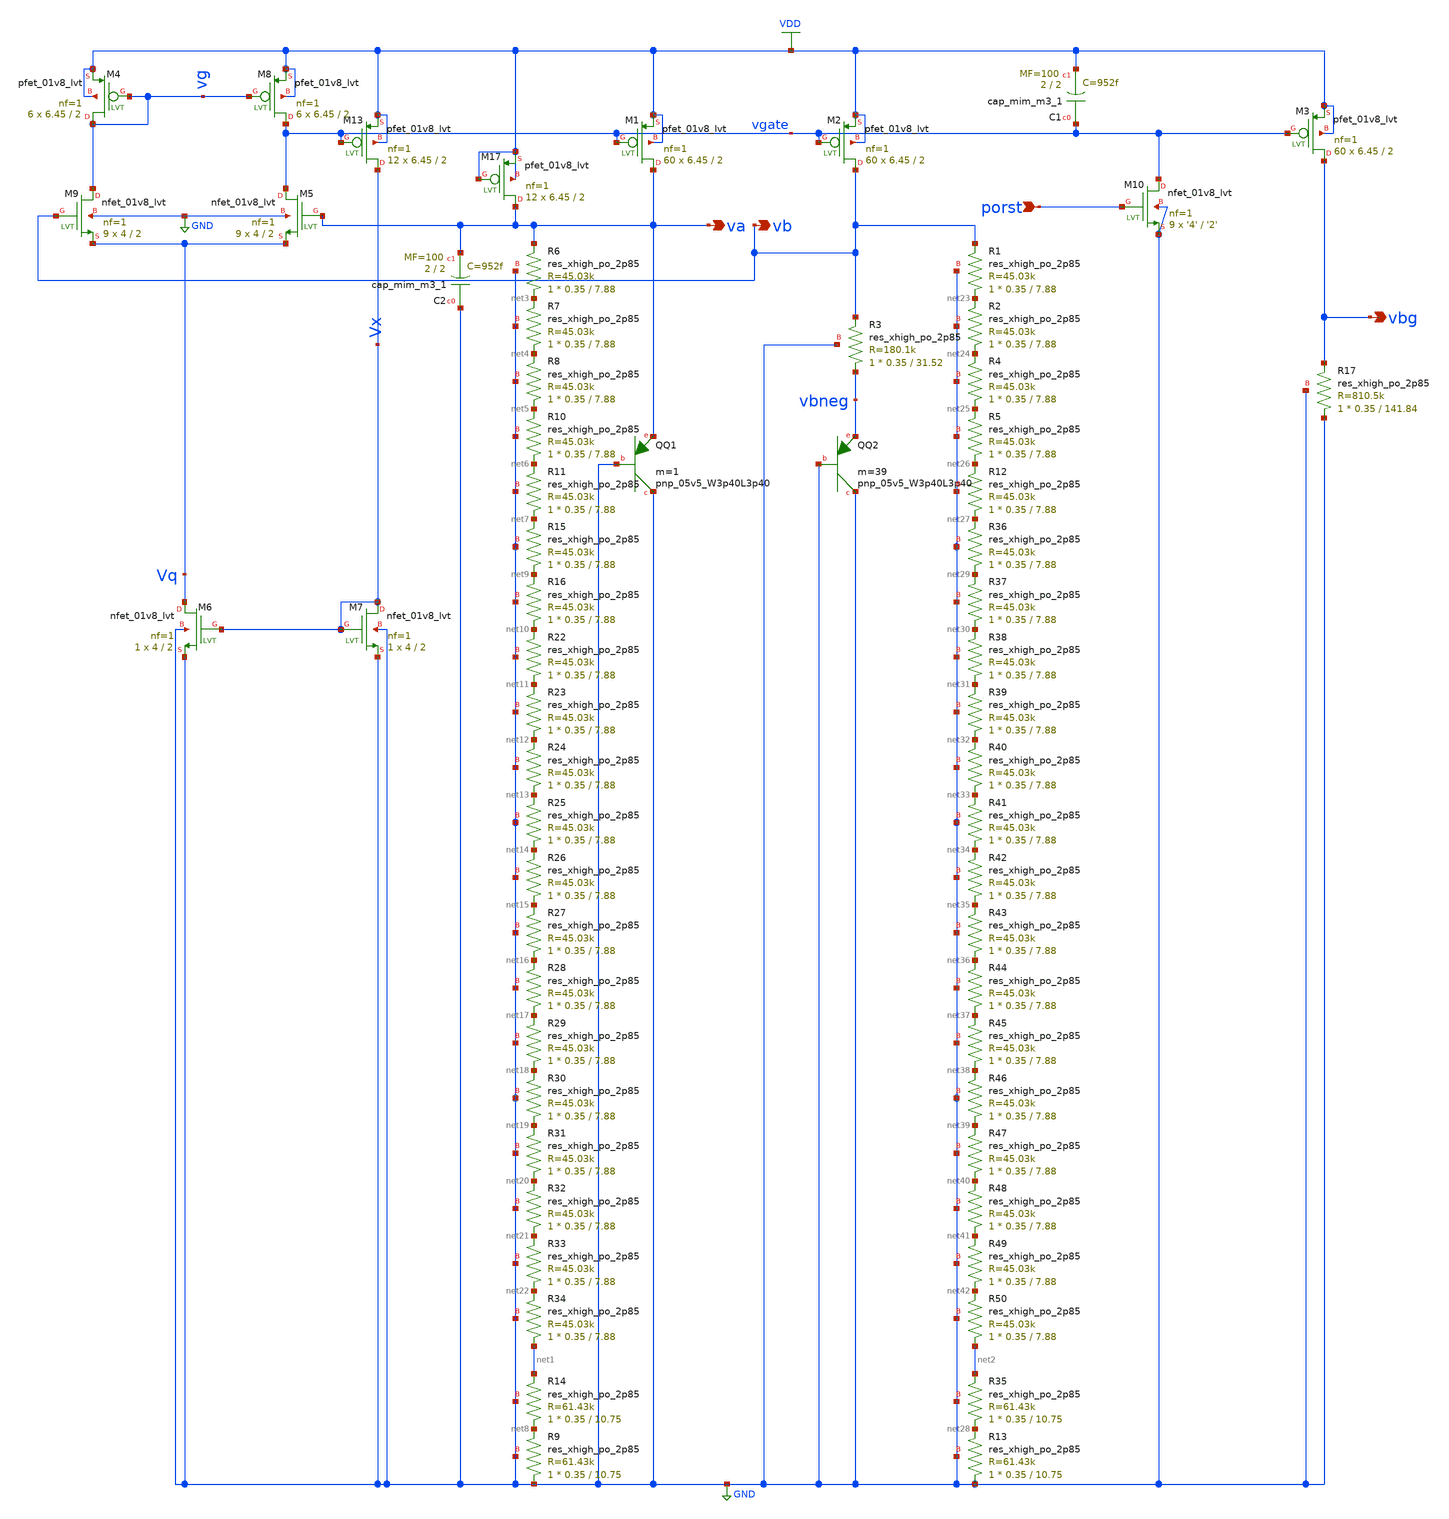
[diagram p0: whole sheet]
** sch_path: schematic/tsmc_bandgap_real_lvs.sch
**.subckt tsmc_bandgap_real_lvs porst vbg va vb
*.ipin porst
*.opin vbg
*.opin va
*.opin vb
XM5 vgate va Vq GND sky130_fd_pr__nfet_01v8_lvt L=2 W=4 nf=1 ad='int((nf+1)/2) * W/nf * 0.29' as='int((nf+2)/2) * W/nf * 0.29'
+ pd='2*int((nf+1)/2) * (W/nf + 0.29)' ps='2*int((nf+2)/2) * (W/nf + 0.29)' nrd='0.29 / W' nrs='0.29 / W'
+ sa=0 sb=0 sd=0 mult=9 m=9
XM6 Vq Vx GND GND sky130_fd_pr__nfet_01v8_lvt L=2 W=4 nf=1 ad='int((nf+1)/2) * W/nf * 0.29' as='int((nf+2)/2) * W/nf * 0.29'
+ pd='2*int((nf+1)/2) * (W/nf + 0.29)' ps='2*int((nf+2)/2) * (W/nf + 0.29)' nrd='0.29 / W' nrs='0.29 / W'
+ sa=0 sb=0 sd=0 mult=1 m=1
XM9 vg vb Vq GND sky130_fd_pr__nfet_01v8_lvt L=2 W=4 nf=1 ad='int((nf+1)/2) * W/nf * 0.29' as='int((nf+2)/2) * W/nf * 0.29'
+ pd='2*int((nf+1)/2) * (W/nf + 0.29)' ps='2*int((nf+2)/2) * (W/nf + 0.29)' nrd='0.29 / W' nrs='0.29 / W'
+ sa=0 sb=0 sd=0 mult=9 m=9
XM7 Vx Vx GND GND sky130_fd_pr__nfet_01v8_lvt L=2 W=4 nf=1 ad='int((nf+1)/2) * W/nf * 0.29' as='int((nf+2)/2) * W/nf * 0.29'
+ pd='2*int((nf+1)/2) * (W/nf + 0.29)' ps='2*int((nf+2)/2) * (W/nf + 0.29)' nrd='0.29 / W' nrs='0.29 / W'
+ sa=0 sb=0 sd=0 mult=1 m=1
XM13 Vx vgate VDD VDD sky130_fd_pr__pfet_01v8_lvt L=2 W=6.45 nf=1 ad='int((nf+1)/2) * W/nf * 0.29' as='int((nf+2)/2) * W/nf * 0.29'
+ pd='2*int((nf+1)/2) * (W/nf + 0.29)' ps='2*int((nf+2)/2) * (W/nf + 0.29)' nrd='0.29 / W' nrs='0.29 / W'
+ sa=0 sb=0 sd=0 mult=12 m=12
XM1 va vgate VDD VDD sky130_fd_pr__pfet_01v8_lvt L=2 W=6.45 nf=1 ad='int((nf+1)/2) * W/nf * 0.29' as='int((nf+2)/2) * W/nf * 0.29'
+ pd='2*int((nf+1)/2) * (W/nf + 0.29)' ps='2*int((nf+2)/2) * (W/nf + 0.29)' nrd='0.29 / W' nrs='0.29 / W'
+ sa=0 sb=0 sd=0 mult=60 m=60
XM2 vb vgate VDD VDD sky130_fd_pr__pfet_01v8_lvt L=2 W=6.45 nf=1 ad='int((nf+1)/2) * W/nf * 0.29' as='int((nf+2)/2) * W/nf * 0.29'
+ pd='2*int((nf+1)/2) * (W/nf + 0.29)' ps='2*int((nf+2)/2) * (W/nf + 0.29)' nrd='0.29 / W' nrs='0.29 / W'
+ sa=0 sb=0 sd=0 mult=60 m=60
XM3 vbg vgate VDD VDD sky130_fd_pr__pfet_01v8_lvt L=2 W=6.45 nf=1 ad='int((nf+1)/2) * W/nf * 0.29' as='int((nf+2)/2) * W/nf * 0.29'
+ pd='2*int((nf+1)/2) * (W/nf + 0.29)' ps='2*int((nf+2)/2) * (W/nf + 0.29)' nrd='0.29 / W' nrs='0.29 / W'
+ sa=0 sb=0 sd=0 mult=60 m=60
XM4 vg vg VDD VDD sky130_fd_pr__pfet_01v8_lvt L=2 W=6.45 nf=1 ad='int((nf+1)/2) * W/nf * 0.29' as='int((nf+2)/2) * W/nf * 0.29'
+ pd='2*int((nf+1)/2) * (W/nf + 0.29)' ps='2*int((nf+2)/2) * (W/nf + 0.29)' nrd='0.29 / W' nrs='0.29 / W'
+ sa=0 sb=0 sd=0 mult=6 m=6
XM8 vgate vg VDD VDD sky130_fd_pr__pfet_01v8_lvt L=2 W=6.45 nf=1 ad='int((nf+1)/2) * W/nf * 0.29' as='int((nf+2)/2) * W/nf * 0.29'
+ pd='2*int((nf+1)/2) * (W/nf + 0.29)' ps='2*int((nf+2)/2) * (W/nf + 0.29)' nrd='0.29 / W' nrs='0.29 / W'
+ sa=0 sb=0 sd=0 mult=6 m=6
XM10 vgate porst GND GND sky130_fd_pr__nfet_01v8_lvt L='2' W='4' nf=1 ad='int((nf+1)/2) * W/nf * 0.29'
+ as='int((nf+2)/2) * W/nf * 0.29' pd='2*int((nf+1)/2) * (W/nf + 0.29)' ps='2*int((nf+2)/2) * (W/nf + 0.29)'
+ nrd='0.29 / W' nrs='0.29 / W' sa=0 sb=0 sd=0 mult=9 m=9
XR6 net3 va GND sky130_fd_pr__res_xhigh_po_2p85 L=7.88 mult=1 m=1
XR7 net4 net3 GND sky130_fd_pr__res_xhigh_po_2p85 L=7.88 mult=1 m=1
XR8 net5 net4 GND sky130_fd_pr__res_xhigh_po_2p85 L=7.88 mult=1 m=1
XR10 net6 net5 GND sky130_fd_pr__res_xhigh_po_2p85 L=7.88 mult=1 m=1
XR11 net7 net6 GND sky130_fd_pr__res_xhigh_po_2p85 L=7.88 mult=1 m=1
XR9 GND net8 GND sky130_fd_pr__res_xhigh_po_2p85 L=10.75 mult=1 m=1
XR3 vbneg vb GND sky130_fd_pr__res_xhigh_po_2p85 L=31.52 mult=1 m=1
XR17 GND vbg GND sky130_fd_pr__res_xhigh_po_2p85 L=141.84 mult=1 m=1
XM17 va VDD VDD VDD sky130_fd_pr__pfet_01v8_lvt L=2 W=6.45 nf=1 ad='int((nf+1)/2) * W/nf * 0.29' as='int((nf+2)/2) * W/nf * 0.29'
+ pd='2*int((nf+1)/2) * (W/nf + 0.29)' ps='2*int((nf+2)/2) * (W/nf + 0.29)' nrd='0.29 / W' nrs='0.29 / W'
+ sa=0 sb=0 sd=0 mult=12 m=12
XC1 vgate VDD sky130_fd_pr__cap_mim_m3_1 W=2 L=2 MF=100 m=100
XQQ1 GND GND va sky130_fd_pr__pnp_05v5_W3p40L3p40 m=1
XQQ2 GND GND vbneg sky130_fd_pr__pnp_05v5_W3p40L3p40 m=39
XC2 GND va sky130_fd_pr__cap_mim_m3_1 W=2 L=2 MF=100 m=100
XR14 net8 net1 GND sky130_fd_pr__res_xhigh_po_2p85 L=10.75 mult=1 m=1
XR15 net9 net7 GND sky130_fd_pr__res_xhigh_po_2p85 L=7.88 mult=1 m=1
XR16 net10 net9 GND sky130_fd_pr__res_xhigh_po_2p85 L=7.88 mult=1 m=1
XR22 net11 net10 GND sky130_fd_pr__res_xhigh_po_2p85 L=7.88 mult=1 m=1
XR23 net12 net11 GND sky130_fd_pr__res_xhigh_po_2p85 L=7.88 mult=1 m=1
XR24 net13 net12 GND sky130_fd_pr__res_xhigh_po_2p85 L=7.88 mult=1 m=1
XR25 net14 net13 GND sky130_fd_pr__res_xhigh_po_2p85 L=7.88 mult=1 m=1
XR26 net15 net14 GND sky130_fd_pr__res_xhigh_po_2p85 L=7.88 mult=1 m=1
XR27 net16 net15 GND sky130_fd_pr__res_xhigh_po_2p85 L=7.88 mult=1 m=1
XR28 net17 net16 GND sky130_fd_pr__res_xhigh_po_2p85 L=7.88 mult=1 m=1
XR29 net18 net17 GND sky130_fd_pr__res_xhigh_po_2p85 L=7.88 mult=1 m=1
XR30 net19 net18 GND sky130_fd_pr__res_xhigh_po_2p85 L=7.88 mult=1 m=1
XR31 net20 net19 GND sky130_fd_pr__res_xhigh_po_2p85 L=7.88 mult=1 m=1
XR32 net21 net20 GND sky130_fd_pr__res_xhigh_po_2p85 L=7.88 mult=1 m=1
XR33 net22 net21 GND sky130_fd_pr__res_xhigh_po_2p85 L=7.88 mult=1 m=1
XR34 net1 net22 GND sky130_fd_pr__res_xhigh_po_2p85 L=7.88 mult=1 m=1
XR1 net23 vb GND sky130_fd_pr__res_xhigh_po_2p85 L=7.88 mult=1 m=1
XR2 net24 net23 GND sky130_fd_pr__res_xhigh_po_2p85 L=7.88 mult=1 m=1
XR4 net25 net24 GND sky130_fd_pr__res_xhigh_po_2p85 L=7.88 mult=1 m=1
XR5 net26 net25 GND sky130_fd_pr__res_xhigh_po_2p85 L=7.88 mult=1 m=1
XR12 net27 net26 GND sky130_fd_pr__res_xhigh_po_2p85 L=7.88 mult=1 m=1
XR13 GND net28 GND sky130_fd_pr__res_xhigh_po_2p85 L=10.75 mult=1 m=1
XR35 net28 net2 GND sky130_fd_pr__res_xhigh_po_2p85 L=10.75 mult=1 m=1
XR36 net29 net27 GND sky130_fd_pr__res_xhigh_po_2p85 L=7.88 mult=1 m=1
XR37 net30 net29 GND sky130_fd_pr__res_xhigh_po_2p85 L=7.88 mult=1 m=1
XR38 net31 net30 GND sky130_fd_pr__res_xhigh_po_2p85 L=7.88 mult=1 m=1
XR39 net32 net31 GND sky130_fd_pr__res_xhigh_po_2p85 L=7.88 mult=1 m=1
XR40 net33 net32 GND sky130_fd_pr__res_xhigh_po_2p85 L=7.88 mult=1 m=1
XR41 net34 net33 GND sky130_fd_pr__res_xhigh_po_2p85 L=7.88 mult=1 m=1
XR42 net35 net34 GND sky130_fd_pr__res_xhigh_po_2p85 L=7.88 mult=1 m=1
XR43 net36 net35 GND sky130_fd_pr__res_xhigh_po_2p85 L=7.88 mult=1 m=1
XR44 net37 net36 GND sky130_fd_pr__res_xhigh_po_2p85 L=7.88 mult=1 m=1
XR45 net38 net37 GND sky130_fd_pr__res_xhigh_po_2p85 L=7.88 mult=1 m=1
XR46 net39 net38 GND sky130_fd_pr__res_xhigh_po_2p85 L=7.88 mult=1 m=1
XR47 net40 net39 GND sky130_fd_pr__res_xhigh_po_2p85 L=7.88 mult=1 m=1
XR48 net41 net40 GND sky130_fd_pr__res_xhigh_po_2p85 L=7.88 mult=1 m=1
XR49 net42 net41 GND sky130_fd_pr__res_xhigh_po_2p85 L=7.88 mult=1 m=1
XR50 net2 net42 GND sky130_fd_pr__res_xhigh_po_2p85 L=7.88 mult=1 m=1
**.ends
.GLOBAL GND
.GLOBAL VDD
.end
